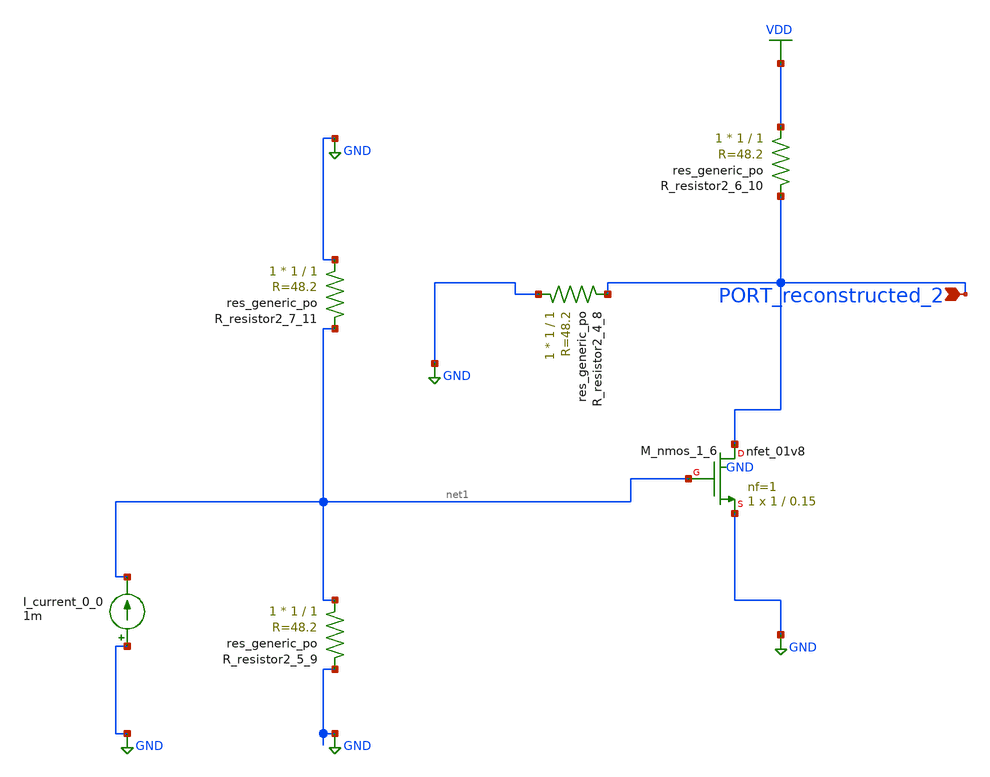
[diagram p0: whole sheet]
** sch_path: schematics/AMSNet/582.sch
**.subckt 582 PORT_reconstructed_2
*.ipin PORT_reconstructed_2
I_current_0_0 GND net1 1m
XM_nmos_1_6 PORT_reconstructed_2 net1 GND GND sky130_fd_pr__nfet_01v8 L=0.15 W=1 nf=1 ad='int((1 + 1)/2) * 1 / 1 * 0.29'
+ as='int((1 + 2)/2) * 1 / 1 * 0.29' pd='2*int((1 + 1)/2) * (1 / 1 + 0.29)' ps='2*int((1 + 2)/2) * (1 / 1 + 0.29)'
+ nrd='0.29 / 1 ' nrs='0.29 / 1 ' sa=0 sb=0 sd=0 mult=1 m=1
XR_resistor2_4_8 GND PORT_reconstructed_2 sky130_fd_pr__res_generic_po W=1 L=1 m=1
XR_resistor2_5_9 net1 GND sky130_fd_pr__res_generic_po W=1 L=1 m=1
XR_resistor2_6_10 VDD PORT_reconstructed_2 sky130_fd_pr__res_generic_po W=1 L=1 m=1
XR_resistor2_7_11 GND net1 sky130_fd_pr__res_generic_po W=1 L=1 m=1
**.ends
.GLOBAL GND
.GLOBAL VDD
.end
